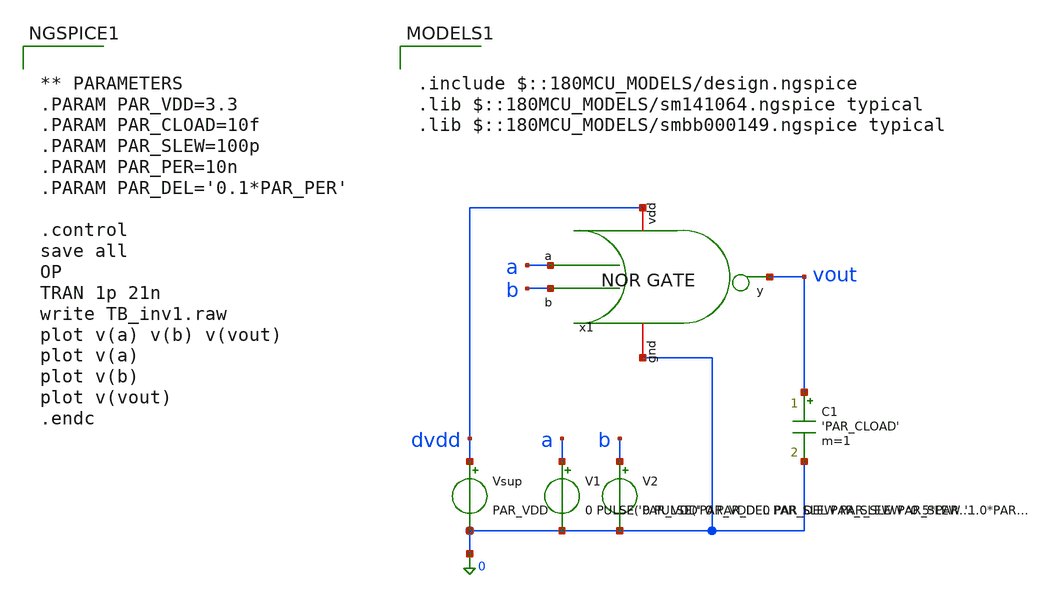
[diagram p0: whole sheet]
** sch_path: src/schematic/NOR/TB_norGate.sch
**.subckt TB_norGate
x1 dvdd a b vout 0 norGate
V1 a 0 0 PULSE('PAR_VDD' 0 PAR_DEL PAR_SLEW PAR_SLEW '0.5*PAR_PER' '1.0*PAR_PER')
Vsup dvdd 0 PAR_VDD
C1 vout 0 'PAR_CLOAD' m=1
V2 b 0 0 PULSE('PAR_VDD' 0 PAR_DEL PAR_SLEW PAR_SLEW '1.0*PAR_PER' '2.0*PAR_PER')
**** begin user architecture code

.include $::180MCU_MODELS/design.ngspice
.lib $::180MCU_MODELS/sm141064.ngspice typical
.lib $::180MCU_MODELS/smbb000149.ngspice typical



** PARAMETERS
.PARAM PAR_VDD=3.3
.PARAM PAR_CLOAD=10f
.PARAM PAR_SLEW=100p
.PARAM PAR_PER=10n
.PARAM PAR_DEL='0.1*PAR_PER'

.control
save all
OP
TRAN 1p 21n
write TB_inv1.raw
plot v(a) v(b) v(vout)
plot v(a)
plot v(b)
plot v(vout)
.endc


**** end user architecture code
**.ends

* expanding   symbol:  src/schematic/NOR/norGate.sym # of pins=5
** sym_path: src/schematic/NOR/norGate.sym
** sch_path: src/schematic/NOR/norGate.sch
.subckt norGate vdd a b y gnd
*.iopin gnd
*.iopin vdd
*.ipin a
*.ipin b
*.opin y
XM1 y a net1 vdd pfet_03v3 L=0.28u W=0.22u nf=1 ad='int((nf+1)/2) * W/nf * 0.18u' as='int((nf+2)/2) * W/nf * 0.18u'
+ pd='2*int((nf+1)/2) * (W/nf + 0.18u)' ps='2*int((nf+2)/2) * (W/nf + 0.18u)' nrd='0.18u / W' nrs='0.18u / W'
+ sa=0 sb=0 sd=0 m=1
XM2 net1 a vdd vdd pfet_03v3 L=0.28u W=0.22u nf=1 ad='int((nf+1)/2) * W/nf * 0.18u' as='int((nf+2)/2) * W/nf * 0.18u'
+ pd='2*int((nf+1)/2) * (W/nf + 0.18u)' ps='2*int((nf+2)/2) * (W/nf + 0.18u)' nrd='0.18u / W' nrs='0.18u / W'
+ sa=0 sb=0 sd=0 m=1
XM3 y a gnd gnd nfet_03v3 L=0.28u W=0.22u nf=1 ad='int((nf+1)/2) * W/nf * 0.18u' as='int((nf+2)/2) * W/nf * 0.18u'
+ pd='2*int((nf+1)/2) * (W/nf + 0.18u)' ps='2*int((nf+2)/2) * (W/nf + 0.18u)' nrd='0.18u / W' nrs='0.18u / W'
+ sa=0 sb=0 sd=0 m=1
XM4 y a gnd gnd nfet_03v3 L=0.28u W=0.22u nf=1 ad='int((nf+1)/2) * W/nf * 0.18u' as='int((nf+2)/2) * W/nf * 0.18u'
+ pd='2*int((nf+1)/2) * (W/nf + 0.18u)' ps='2*int((nf+2)/2) * (W/nf + 0.18u)' nrd='0.18u / W' nrs='0.18u / W'
+ sa=0 sb=0 sd=0 m=1
.ends

.end
